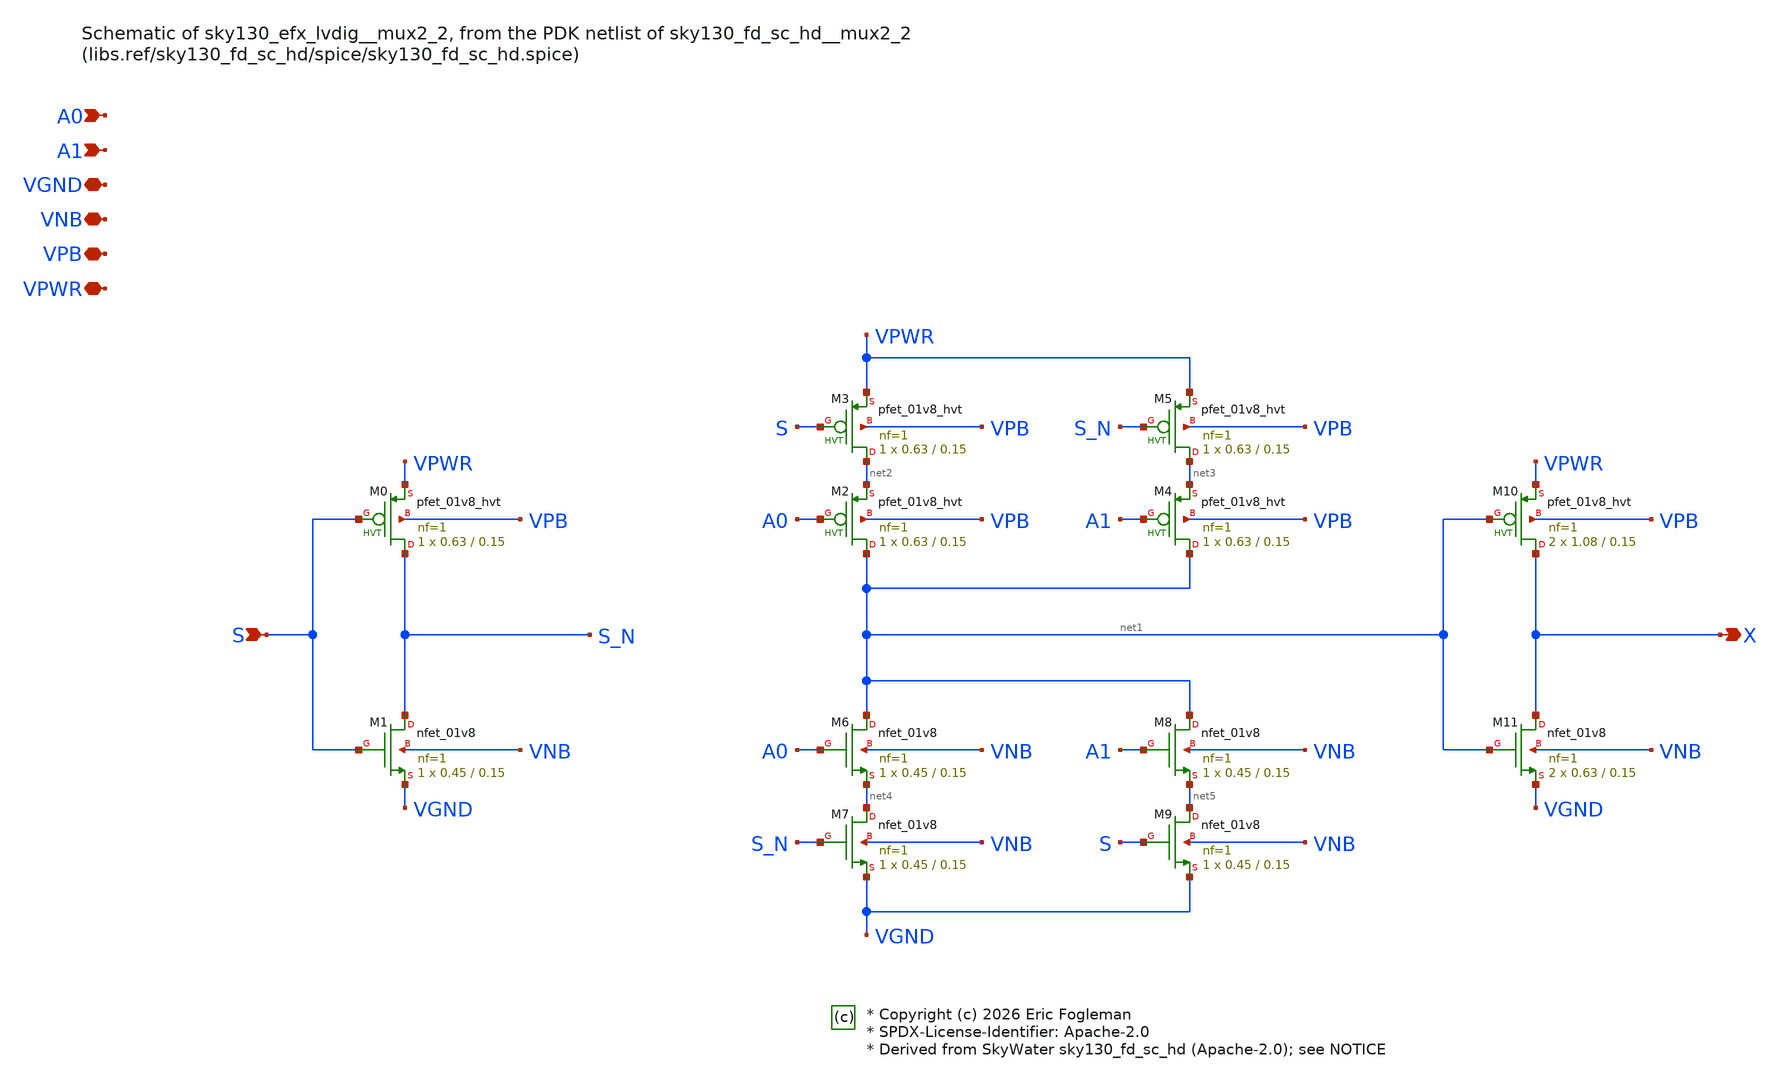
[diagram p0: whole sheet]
** sch_path: xschem/sky130_efx_lvdig__mux2_2.sch

* Copyright (c) 2026 Eric Fogleman
* SPDX-License-Identifier: Apache-2.0
* Derived from SkyWater sky130_fd_sc_hd (Apache-2.0); see NOTICE

**.subckt sky130_efx_lvdig__mux2_2 S X A0 A1 VGND VNB VPB VPWR
*.ipin S
*.opin X
*.ipin A0
*.ipin A1
*.iopin VGND
*.iopin VNB
*.iopin VPB
*.iopin VPWR
XM0 S_N S VPWR VPB sky130_fd_pr__pfet_01v8_hvt L=0.15 W=0.63 nf=1 ad='int((1 + 1)/2) * 0.63 / 1 * 0.29'
+ as='int((1 + 2)/2) * 0.63 / 1 * 0.29' pd='2*int((1 + 1)/2) * (0.63 / 1 + 0.29)' ps='2*int((1 + 2)/2) * (0.63 / 1 + 0.29)'
+ nrd='0.29 / 0.63 ' nrs='0.29 / 0.63 ' sa=0 sb=0 sd=0 mult=1 m=1
XM1 S_N S VGND VNB sky130_fd_pr__nfet_01v8 L=0.15 W=0.45 nf=1 ad='int((1 + 1)/2) * 0.45 / 1 * 0.29' as='int((1 + 2)/2) * 0.45 / 1 * 0.29'
+ pd='2*int((1 + 1)/2) * (0.45 / 1 + 0.29)' ps='2*int((1 + 2)/2) * (0.45 / 1 + 0.29)' nrd='0.29 / 0.45 '
+ nrs='0.29 / 0.45 ' sa=0 sb=0 sd=0 mult=1 m=1
XM2 net1 A0 net2 VPB sky130_fd_pr__pfet_01v8_hvt L=0.15 W=0.63 nf=1 ad='int((1 + 1)/2) * 0.63 / 1 * 0.29'
+ as='int((1 + 2)/2) * 0.63 / 1 * 0.29' pd='2*int((1 + 1)/2) * (0.63 / 1 + 0.29)' ps='2*int((1 + 2)/2) * (0.63 / 1 + 0.29)'
+ nrd='0.29 / 0.63 ' nrs='0.29 / 0.63 ' sa=0 sb=0 sd=0 mult=1 m=1
XM3 net2 S VPWR VPB sky130_fd_pr__pfet_01v8_hvt L=0.15 W=0.63 nf=1 ad='int((1 + 1)/2) * 0.63 / 1 * 0.29'
+ as='int((1 + 2)/2) * 0.63 / 1 * 0.29' pd='2*int((1 + 1)/2) * (0.63 / 1 + 0.29)' ps='2*int((1 + 2)/2) * (0.63 / 1 + 0.29)'
+ nrd='0.29 / 0.63 ' nrs='0.29 / 0.63 ' sa=0 sb=0 sd=0 mult=1 m=1
XM4 net1 A1 net3 VPB sky130_fd_pr__pfet_01v8_hvt L=0.15 W=0.63 nf=1 ad='int((1 + 1)/2) * 0.63 / 1 * 0.29'
+ as='int((1 + 2)/2) * 0.63 / 1 * 0.29' pd='2*int((1 + 1)/2) * (0.63 / 1 + 0.29)' ps='2*int((1 + 2)/2) * (0.63 / 1 + 0.29)'
+ nrd='0.29 / 0.63 ' nrs='0.29 / 0.63 ' sa=0 sb=0 sd=0 mult=1 m=1
XM5 net3 S_N VPWR VPB sky130_fd_pr__pfet_01v8_hvt L=0.15 W=0.63 nf=1 ad='int((1 + 1)/2) * 0.63 / 1 * 0.29'
+ as='int((1 + 2)/2) * 0.63 / 1 * 0.29' pd='2*int((1 + 1)/2) * (0.63 / 1 + 0.29)' ps='2*int((1 + 2)/2) * (0.63 / 1 + 0.29)'
+ nrd='0.29 / 0.63 ' nrs='0.29 / 0.63 ' sa=0 sb=0 sd=0 mult=1 m=1
XM6 net1 A0 net4 VNB sky130_fd_pr__nfet_01v8 L=0.15 W=0.45 nf=1 ad='int((1 + 1)/2) * 0.45 / 1 * 0.29'
+ as='int((1 + 2)/2) * 0.45 / 1 * 0.29' pd='2*int((1 + 1)/2) * (0.45 / 1 + 0.29)' ps='2*int((1 + 2)/2) * (0.45 / 1 + 0.29)'
+ nrd='0.29 / 0.45 ' nrs='0.29 / 0.45 ' sa=0 sb=0 sd=0 mult=1 m=1
XM7 net4 S_N VGND VNB sky130_fd_pr__nfet_01v8 L=0.15 W=0.45 nf=1 ad='int((1 + 1)/2) * 0.45 / 1 * 0.29'
+ as='int((1 + 2)/2) * 0.45 / 1 * 0.29' pd='2*int((1 + 1)/2) * (0.45 / 1 + 0.29)' ps='2*int((1 + 2)/2) * (0.45 / 1 + 0.29)'
+ nrd='0.29 / 0.45 ' nrs='0.29 / 0.45 ' sa=0 sb=0 sd=0 mult=1 m=1
XM8 net1 A1 net5 VNB sky130_fd_pr__nfet_01v8 L=0.15 W=0.45 nf=1 ad='int((1 + 1)/2) * 0.45 / 1 * 0.29'
+ as='int((1 + 2)/2) * 0.45 / 1 * 0.29' pd='2*int((1 + 1)/2) * (0.45 / 1 + 0.29)' ps='2*int((1 + 2)/2) * (0.45 / 1 + 0.29)'
+ nrd='0.29 / 0.45 ' nrs='0.29 / 0.45 ' sa=0 sb=0 sd=0 mult=1 m=1
XM9 net5 S VGND VNB sky130_fd_pr__nfet_01v8 L=0.15 W=0.45 nf=1 ad='int((1 + 1)/2) * 0.45 / 1 * 0.29'
+ as='int((1 + 2)/2) * 0.45 / 1 * 0.29' pd='2*int((1 + 1)/2) * (0.45 / 1 + 0.29)' ps='2*int((1 + 2)/2) * (0.45 / 1 + 0.29)'
+ nrd='0.29 / 0.45 ' nrs='0.29 / 0.45 ' sa=0 sb=0 sd=0 mult=1 m=1
XM10 X net1 VPWR VPB sky130_fd_pr__pfet_01v8_hvt L=0.15 W=1.08 nf=1 ad='int((1 + 1)/2) * 1.08 / 1 * 0.29'
+ as='int((1 + 2)/2) * 1.08 / 1 * 0.29' pd='2*int((1 + 1)/2) * (1.08 / 1 + 0.29)' ps='2*int((1 + 2)/2) * (1.08 / 1 + 0.29)'
+ nrd='0.29 / 1.08 ' nrs='0.29 / 1.08 ' sa=0 sb=0 sd=0 mult=2 m=2
XM11 X net1 VGND VNB sky130_fd_pr__nfet_01v8 L=0.15 W=0.63 nf=1 ad='int((1 + 1)/2) * 0.63 / 1 * 0.29'
+ as='int((1 + 2)/2) * 0.63 / 1 * 0.29' pd='2*int((1 + 1)/2) * (0.63 / 1 + 0.29)' ps='2*int((1 + 2)/2) * (0.63 / 1 + 0.29)'
+ nrd='0.29 / 0.63 ' nrs='0.29 / 0.63 ' sa=0 sb=0 sd=0 mult=2 m=2
**.ends
.end
